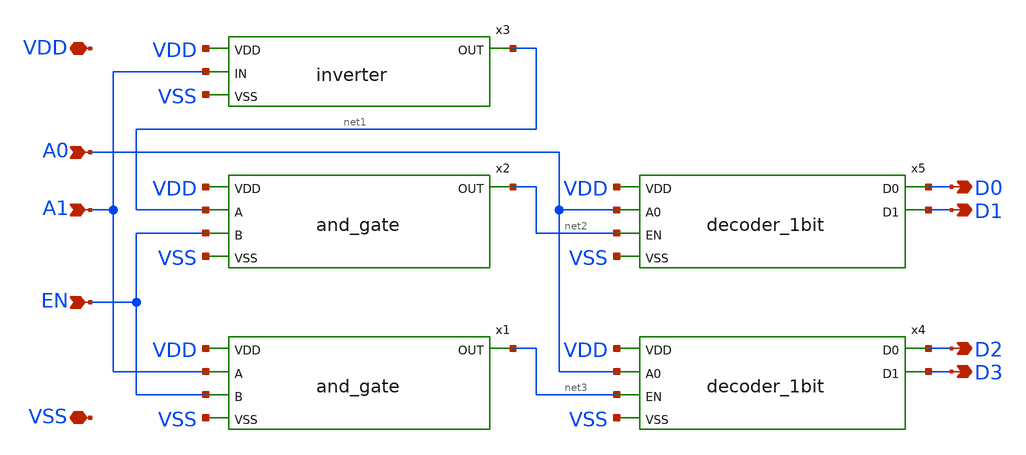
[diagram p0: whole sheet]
** sch_path: xschem/decoder_2bit.sch
**.subckt decoder_2bit VSS VDD A0 EN D0 D1 A1 D2 D3
*.iopin VSS
*.iopin VDD
*.ipin A0
*.ipin EN
*.opin D0
*.opin D1
*.ipin A1
*.opin D2
*.opin D3
x1 VDD net3 A1 EN VSS and_gate
x2 VDD net2 net1 EN VSS and_gate
x3 VDD A1 net1 VSS inverter
x4 VDD D2 A0 net3 D3 VSS decoder_1bit
x5 VDD D0 A0 net2 D1 VSS decoder_1bit
**.ends
.end
